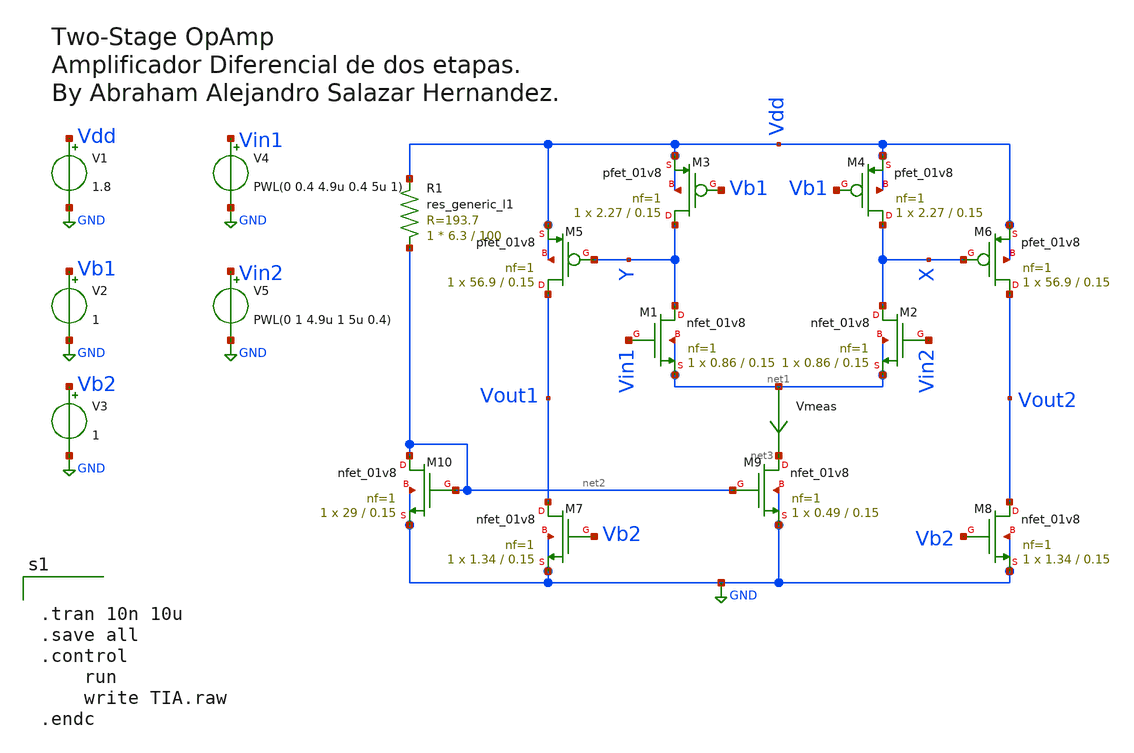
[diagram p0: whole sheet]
** sch_path: TIA/TIA.sch
**.subckt TIA
XM1 Y Vin1 net1 net1 sky130_fd_pr__nfet_01v8 L=0.15 W=0.86 nf=1 ad='int((nf+1)/2) * W/nf * 0.29' as='int((nf+2)/2) * W/nf * 0.29'
+ pd='2*int((nf+1)/2) * (W/nf + 0.29)' ps='2*int((nf+2)/2) * (W/nf + 0.29)' nrd='0.29 / W' nrs='0.29 / W'
+ sa=0 sb=0 sd=0 mult=1 m=1
XM2 X Vin2 net1 net1 sky130_fd_pr__nfet_01v8 L=0.15 W=0.86 nf=1 ad='int((nf+1)/2) * W/nf * 0.29' as='int((nf+2)/2) * W/nf * 0.29'
+ pd='2*int((nf+1)/2) * (W/nf + 0.29)' ps='2*int((nf+2)/2) * (W/nf + 0.29)' nrd='0.29 / W' nrs='0.29 / W'
+ sa=0 sb=0 sd=0 mult=1 m=1
XM3 Y Vb1 Vdd Vdd sky130_fd_pr__pfet_01v8 L=0.15 W=2.27 nf=1 ad='int((nf+1)/2) * W/nf * 0.29' as='int((nf+2)/2) * W/nf * 0.29'
+ pd='2*int((nf+1)/2) * (W/nf + 0.29)' ps='2*int((nf+2)/2) * (W/nf + 0.29)' nrd='0.29 / W' nrs='0.29 / W'
+ sa=0 sb=0 sd=0 mult=1 m=1
XM4 X Vb1 Vdd Vdd sky130_fd_pr__pfet_01v8 L=0.15 W=2.27 nf=1 ad='int((nf+1)/2) * W/nf * 0.29' as='int((nf+2)/2) * W/nf * 0.29'
+ pd='2*int((nf+1)/2) * (W/nf + 0.29)' ps='2*int((nf+2)/2) * (W/nf + 0.29)' nrd='0.29 / W' nrs='0.29 / W'
+ sa=0 sb=0 sd=0 mult=1 m=1
XM5 Vout1 Y Vdd Vdd sky130_fd_pr__pfet_01v8 L=0.15 W=56.9 nf=1 ad='int((nf+1)/2) * W/nf * 0.29' as='int((nf+2)/2) * W/nf * 0.29'
+ pd='2*int((nf+1)/2) * (W/nf + 0.29)' ps='2*int((nf+2)/2) * (W/nf + 0.29)' nrd='0.29 / W' nrs='0.29 / W'
+ sa=0 sb=0 sd=0 mult=1 m=1
XM6 Vout2 X Vdd Vdd sky130_fd_pr__pfet_01v8 L=0.15 W=56.9 nf=1 ad='int((nf+1)/2) * W/nf * 0.29' as='int((nf+2)/2) * W/nf * 0.29'
+ pd='2*int((nf+1)/2) * (W/nf + 0.29)' ps='2*int((nf+2)/2) * (W/nf + 0.29)' nrd='0.29 / W' nrs='0.29 / W'
+ sa=0 sb=0 sd=0 mult=1 m=1
XM7 Vout1 Vb2 GND GND sky130_fd_pr__nfet_01v8 L=0.15 W=1.34 nf=1 ad='int((nf+1)/2) * W/nf * 0.29' as='int((nf+2)/2) * W/nf * 0.29'
+ pd='2*int((nf+1)/2) * (W/nf + 0.29)' ps='2*int((nf+2)/2) * (W/nf + 0.29)' nrd='0.29 / W' nrs='0.29 / W'
+ sa=0 sb=0 sd=0 mult=1 m=1
XM8 Vout2 Vb2 GND GND sky130_fd_pr__nfet_01v8 L=0.15 W=1.34 nf=1 ad='int((nf+1)/2) * W/nf * 0.29' as='int((nf+2)/2) * W/nf * 0.29'
+ pd='2*int((nf+1)/2) * (W/nf + 0.29)' ps='2*int((nf+2)/2) * (W/nf + 0.29)' nrd='0.29 / W' nrs='0.29 / W'
+ sa=0 sb=0 sd=0 mult=1 m=1
XM9 net3 net2 GND GND sky130_fd_pr__nfet_01v8 L=0.15 W=0.49 nf=1 ad='int((nf+1)/2) * W/nf * 0.29' as='int((nf+2)/2) * W/nf * 0.29'
+ pd='2*int((nf+1)/2) * (W/nf + 0.29)' ps='2*int((nf+2)/2) * (W/nf + 0.29)' nrd='0.29 / W' nrs='0.29 / W'
+ sa=0 sb=0 sd=0 mult=1 m=1
Vmeas net1 net3 0
.save i(vmeas)
XM10 net2 net2 GND GND sky130_fd_pr__nfet_01v8 L=0.15 W=29 nf=1 ad='int((nf+1)/2) * W/nf * 0.29' as='int((nf+2)/2) * W/nf * 0.29'
+ pd='2*int((nf+1)/2) * (W/nf + 0.29)' ps='2*int((nf+2)/2) * (W/nf + 0.29)' nrd='0.29 / W' nrs='0.29 / W'
+ sa=0 sb=0 sd=0 mult=1 m=1
R1 net2 Vdd sky130_fd_pr__res_generic_l1 W=6.3 L=100 m=1
V1 Vdd GND 1.8
V2 Vb1 GND 1
V3 Vb2 GND 1
V4 Vin1 GND PWL(0 0.4 4.9u 0.4 5u 1)
V5 Vin2 GND PWL(0 1 4.9u 1 5u 0.4)
**** begin user architecture code

** opencircuitdesign pdks install
.lib $::SKYWATER_MODELS/sky130.lib.spice ss




.tran 10n 10u
.save all
.control
	run
	write TIA.raw
.endc


**** end user architecture code
**.ends
.GLOBAL GND
.end
